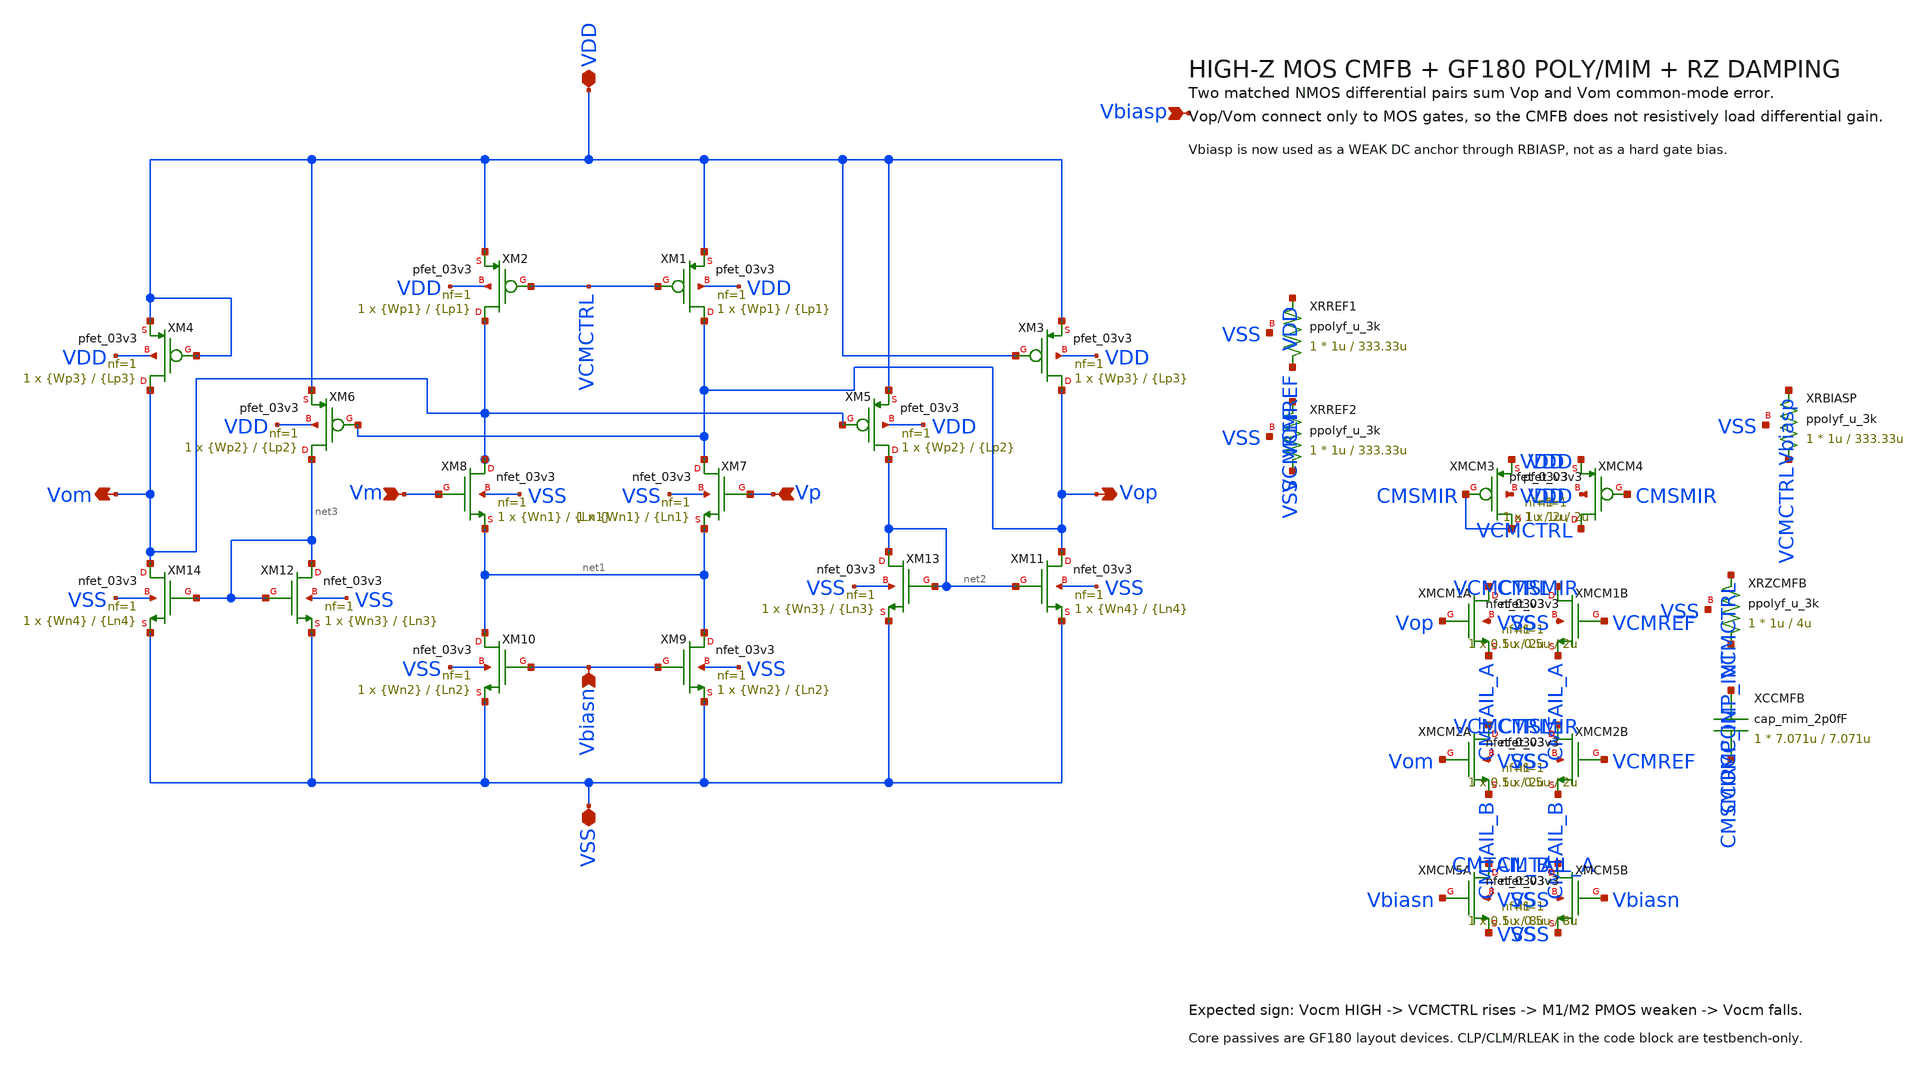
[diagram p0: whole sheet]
** sch_path: src/schematics/TEMPORARY/CMFB_HIGHZ_LAYOUTREADY_RZ12K_C100f_transient.sch
**.subckt CMFB_HIGHZ_LAYOUTREADY_RZ12K_C100f_transient VDD VSS Vbiasn Vbiasp Vm Vp Vom Vop
*.iopin VDD
*.iopin VSS
*.ipin Vbiasn
*.ipin Vbiasp
*.ipin Vm
*.ipin Vp
*.opin Vom
*.opin Vop
XM5 net2 Vom VDD VDD pfet_03v3 L={Lp2} W={Wp2} nf=1 ad='int((nf+1)/2) * W/nf * 0.18u' as='int((nf+2)/2) * W/nf * 0.18u'
+ pd='2*int((nf+1)/2) * (W/nf + 0.18u)' ps='2*int((nf+2)/2) * (W/nf + 0.18u)' nrd='0.18u / W' nrs='0.18u / W'
+ sa=0 sb=0 sd=0 m=1
XM2 Vom VCMCTRL VDD VDD pfet_03v3 L={Lp1} W={Wp1} nf=1 ad='int((nf+1)/2) * W/nf * 0.18u' as='int((nf+2)/2) * W/nf * 0.18u'
+ pd='2*int((nf+1)/2) * (W/nf + 0.18u)' ps='2*int((nf+2)/2) * (W/nf + 0.18u)' nrd='0.18u / W' nrs='0.18u / W'
+ sa=0 sb=0 sd=0 m=1
XM8 Vom Vm net1 VSS nfet_03v3 L={Ln1} W={Wn1} nf=1 ad='int((nf+1)/2) * W/nf * 0.18u' as='int((nf+2)/2) * W/nf * 0.18u'
+ pd='2*int((nf+1)/2) * (W/nf + 0.18u)' ps='2*int((nf+2)/2) * (W/nf + 0.18u)' nrd='0.18u / W' nrs='0.18u / W'
+ sa=0 sb=0 sd=0 m=1
XM7 Vop Vp net1 VSS nfet_03v3 L={Ln1} W={Wn1} nf=1 ad='int((nf+1)/2) * W/nf * 0.18u' as='int((nf+2)/2) * W/nf * 0.18u'
+ pd='2*int((nf+1)/2) * (W/nf + 0.18u)' ps='2*int((nf+2)/2) * (W/nf + 0.18u)' nrd='0.18u / W' nrs='0.18u / W'
+ sa=0 sb=0 sd=0 m=1
XM1 Vop VCMCTRL VDD VDD pfet_03v3 L={Lp1} W={Wp1} nf=1 ad='int((nf+1)/2) * W/nf * 0.18u' as='int((nf+2)/2) * W/nf * 0.18u'
+ pd='2*int((nf+1)/2) * (W/nf + 0.18u)' ps='2*int((nf+2)/2) * (W/nf + 0.18u)' nrd='0.18u / W' nrs='0.18u / W'
+ sa=0 sb=0 sd=0 m=1
XM6 net3 Vop VDD VDD pfet_03v3 L={Lp2} W={Wp2} nf=1 ad='int((nf+1)/2) * W/nf * 0.18u' as='int((nf+2)/2) * W/nf * 0.18u'
+ pd='2*int((nf+1)/2) * (W/nf + 0.18u)' ps='2*int((nf+2)/2) * (W/nf + 0.18u)' nrd='0.18u / W' nrs='0.18u / W'
+ sa=0 sb=0 sd=0 m=1
XM4 Vom VDD VDD VDD pfet_03v3 L={Lp3} W={Wp3} nf=1 ad='int((nf+1)/2) * W/nf * 0.18u' as='int((nf+2)/2) * W/nf * 0.18u'
+ pd='2*int((nf+1)/2) * (W/nf + 0.18u)' ps='2*int((nf+2)/2) * (W/nf + 0.18u)' nrd='0.18u / W' nrs='0.18u / W'
+ sa=0 sb=0 sd=0 m=1
XM3 Vop VDD VDD VDD pfet_03v3 L={Lp3} W={Wp3} nf=1 ad='int((nf+1)/2) * W/nf * 0.18u' as='int((nf+2)/2) * W/nf * 0.18u'
+ pd='2*int((nf+1)/2) * (W/nf + 0.18u)' ps='2*int((nf+2)/2) * (W/nf + 0.18u)' nrd='0.18u / W' nrs='0.18u / W'
+ sa=0 sb=0 sd=0 m=1
XM9 net1 Vbiasn VSS VSS nfet_03v3 L={Ln2} W={Wn2} nf=1 ad='int((nf+1)/2) * W/nf * 0.18u' as='int((nf+2)/2) * W/nf * 0.18u'
+ pd='2*int((nf+1)/2) * (W/nf + 0.18u)' ps='2*int((nf+2)/2) * (W/nf + 0.18u)' nrd='0.18u / W' nrs='0.18u / W'
+ sa=0 sb=0 sd=0 m=1
XM10 net1 Vbiasn VSS VSS nfet_03v3 L={Ln2} W={Wn2} nf=1 ad='int((nf+1)/2) * W/nf * 0.18u' as='int((nf+2)/2) * W/nf * 0.18u'
+ pd='2*int((nf+1)/2) * (W/nf + 0.18u)' ps='2*int((nf+2)/2) * (W/nf + 0.18u)' nrd='0.18u / W' nrs='0.18u / W'
+ sa=0 sb=0 sd=0 m=1
XM11 Vop net2 VSS VSS nfet_03v3 L={Ln4} W={Wn4} nf=1 ad='int((nf+1)/2) * W/nf * 0.18u' as='int((nf+2)/2) * W/nf * 0.18u'
+ pd='2*int((nf+1)/2) * (W/nf + 0.18u)' ps='2*int((nf+2)/2) * (W/nf + 0.18u)' nrd='0.18u / W' nrs='0.18u / W'
+ sa=0 sb=0 sd=0 m=1
XM13 net2 net2 VSS VSS nfet_03v3 L={Ln3} W={Wn3} nf=1 ad='int((nf+1)/2) * W/nf * 0.18u' as='int((nf+2)/2) * W/nf * 0.18u'
+ pd='2*int((nf+1)/2) * (W/nf + 0.18u)' ps='2*int((nf+2)/2) * (W/nf + 0.18u)' nrd='0.18u / W' nrs='0.18u / W'
+ sa=0 sb=0 sd=0 m=1
XM12 net3 net3 VSS VSS nfet_03v3 L={Ln3} W={Wn3} nf=1 ad='int((nf+1)/2) * W/nf * 0.18u' as='int((nf+2)/2) * W/nf * 0.18u'
+ pd='2*int((nf+1)/2) * (W/nf + 0.18u)' ps='2*int((nf+2)/2) * (W/nf + 0.18u)' nrd='0.18u / W' nrs='0.18u / W'
+ sa=0 sb=0 sd=0 m=1
XM14 Vom net3 VSS VSS nfet_03v3 L={Ln4} W={Wn4} nf=1 ad='int((nf+1)/2) * W/nf * 0.18u' as='int((nf+2)/2) * W/nf * 0.18u'
+ pd='2*int((nf+1)/2) * (W/nf + 0.18u)' ps='2*int((nf+2)/2) * (W/nf + 0.18u)' nrd='0.18u / W' nrs='0.18u / W'
+ sa=0 sb=0 sd=0 m=1
XRREF1 VCMREF VDD VSS ppolyf_u_3k r_width=1u r_length=333.33u m=1
XRREF2 VSS VCMREF VSS ppolyf_u_3k r_width=1u r_length=333.33u m=1
XRBIASP VCMCTRL Vbiasp VSS ppolyf_u_3k r_width=1u r_length=333.33u m=1
XMCM3 CMSMIR CMSMIR VDD VDD pfet_03v3 L=2u W=1u nf=1 ad='int((nf+1)/2) * W/nf * 0.18u' as='int((nf+2)/2) * W/nf * 0.18u'
+ pd='2*int((nf+1)/2) * (W/nf + 0.18u)' ps='2*int((nf+2)/2) * (W/nf + 0.18u)' nrd='0.18u / W' nrs='0.18u / W'
+ sa=0 sb=0 sd=0 m=1
XMCM4 VCMCTRL CMSMIR VDD VDD pfet_03v3 L=2u W=1u nf=1 ad='int((nf+1)/2) * W/nf * 0.18u' as='int((nf+2)/2) * W/nf * 0.18u'
+ pd='2*int((nf+1)/2) * (W/nf + 0.18u)' ps='2*int((nf+2)/2) * (W/nf + 0.18u)' nrd='0.18u / W' nrs='0.18u / W'
+ sa=0 sb=0 sd=0 m=1
XMCM1A CMSMIR Vop CMTAIL_A VSS nfet_03v3 L=2u W=0.5u nf=1 ad='int((nf+1)/2) * W/nf * 0.18u' as='int((nf+2)/2) * W/nf * 0.18u'
+ pd='2*int((nf+1)/2) * (W/nf + 0.18u)' ps='2*int((nf+2)/2) * (W/nf + 0.18u)' nrd='0.18u / W' nrs='0.18u / W'
+ sa=0 sb=0 sd=0 m=1
XMCM1B VCMCTRL VCMREF CMTAIL_A VSS nfet_03v3 L=2u W=0.5u nf=1 ad='int((nf+1)/2) * W/nf * 0.18u' as='int((nf+2)/2) * W/nf * 0.18u'
+ pd='2*int((nf+1)/2) * (W/nf + 0.18u)' ps='2*int((nf+2)/2) * (W/nf + 0.18u)' nrd='0.18u / W' nrs='0.18u / W'
+ sa=0 sb=0 sd=0 m=1
XMCM2A CMSMIR Vom CMTAIL_B VSS nfet_03v3 L=2u W=0.5u nf=1 ad='int((nf+1)/2) * W/nf * 0.18u' as='int((nf+2)/2) * W/nf * 0.18u'
+ pd='2*int((nf+1)/2) * (W/nf + 0.18u)' ps='2*int((nf+2)/2) * (W/nf + 0.18u)' nrd='0.18u / W' nrs='0.18u / W'
+ sa=0 sb=0 sd=0 m=1
XMCM2B VCMCTRL VCMREF CMTAIL_B VSS nfet_03v3 L=2u W=0.5u nf=1 ad='int((nf+1)/2) * W/nf * 0.18u' as='int((nf+2)/2) * W/nf * 0.18u'
+ pd='2*int((nf+1)/2) * (W/nf + 0.18u)' ps='2*int((nf+2)/2) * (W/nf + 0.18u)' nrd='0.18u / W' nrs='0.18u / W'
+ sa=0 sb=0 sd=0 m=1
XMCM5A CMTAIL_A Vbiasn VSS VSS nfet_03v3 L=8u W=0.5u nf=1 ad='int((nf+1)/2) * W/nf * 0.18u' as='int((nf+2)/2) * W/nf * 0.18u'
+ pd='2*int((nf+1)/2) * (W/nf + 0.18u)' ps='2*int((nf+2)/2) * (W/nf + 0.18u)' nrd='0.18u / W' nrs='0.18u / W'
+ sa=0 sb=0 sd=0 m=1
XMCM5B CMTAIL_B Vbiasn VSS VSS nfet_03v3 L=8u W=0.5u nf=1 ad='int((nf+1)/2) * W/nf * 0.18u' as='int((nf+2)/2) * W/nf * 0.18u'
+ pd='2*int((nf+1)/2) * (W/nf + 0.18u)' ps='2*int((nf+2)/2) * (W/nf + 0.18u)' nrd='0.18u / W' nrs='0.18u / W'
+ sa=0 sb=0 sd=0 m=1
XRZCMFB CCOMP_INT VCMCTRL VSS ppolyf_u_3k r_width=1u r_length=4u m=1
XCCMFB CCOMP_INT CMSMIR cap_mim_2p0fF c_width=7.071u c_length=7.071u m=1
**** begin user architecture code


.lib /foss/pdks/gf180mcuD/libs.tech/ngspice/sm141064.ngspice typical
.inc /foss/pdks/gf180mcuD/libs.tech/ngspice/design.ngspice

.param Wp1=10u Wp2=1u Wp3=0.5u
.param Wn1=10u Wn2=10u Wn3=5u Wn4=0.5u
.param Lp1=5u Lp2=2u Lp3=5u
.param Ln1=5u Ln2=2u Ln3=0.35u Ln4=15u
.param CL=30f

VTEST_DD VDD 0 3.3
VTEST_SS VSS 0 0
VTEST_BN Vbiasn VSS 0.65
VTEST_BP Vbiasp VSS 2.5
VTEST_VP Vp VSS SIN(1.65 20u 2k 0 0 0)
VTEST_VM Vm VSS SIN(1.65 20u 2k 0 0 180)

CLP Vop VSS 30f
CLM Vom VSS 30f
RLEAKP Vop VSS 1T
RLEAKM Vom VSS 1T

.option reltol=1e-5 abstol=1e-12 vntol=1e-7 temp=27

.control
set color0=white
set color1=black
save all

tran 20n 2m

let vicm=(v(Vp)+v(Vm))/2
let vid=v(Vp)-v(Vm)
let vocm=(v(Vop)+v(Vom))/2
let vod=v(Vop)-v(Vom)
let cmerr=vocm-1.65

meas tran vocm_avg AVG vocm FROM=500u TO=2m
meas tran vocm_max MAX vocm FROM=500u TO=2m
meas tran vocm_min MIN vocm FROM=500u TO=2m
meas tran vod_max MAX vod FROM=500u TO=2m
meas tran vod_min MIN vod FROM=500u TO=2m

set wr_vecnames
set wr_singlescale
wrdata /foss/designs/schematics/TEMPORARY/fullydiffamp_cmfb_HIGHZ_LAYOUTREADY_RZ12K_C100f_tran.txt
+ v(Vp) v(Vm) v(Vop) v(Vom) v(VCMREF) v(CMSMIR) v(VCMCTRL) vicm vid vocm vod cmerr

plot v(Vop) v(Vom)
plot vocm
plot vocm v(VCMREF)
plot v(VCMCTRL)
plot vid vod
.endc


**** end user architecture code
**.ends
.end
